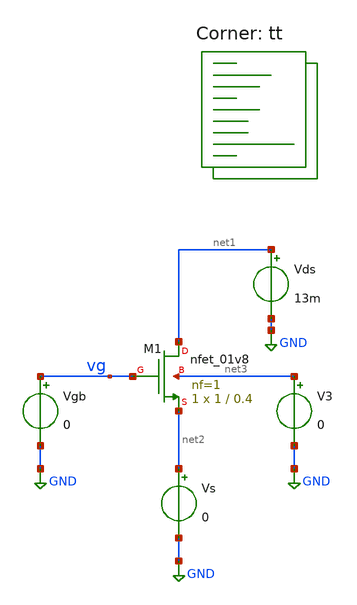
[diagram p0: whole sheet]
** sch_path: legacy/Examples/SkyWater130/xschem/Extraction/nmos_ext.sch
**.subckt nmos_ext
Vgb vg GND 0
Vds net1 GND 13m
V3 net3 GND 0
Vs net2 GND 0
XM1 net1 vg net2 net3 sky130_fd_pr__nfet_01v8 L=0.4 W=1 nf=1 ad='int((nf+1)/2) * W/nf * 0.29' as='int((nf+2)/2) * W/nf * 0.29'
+ pd='2*int((nf+1)/2) * (W/nf + 0.29)' ps='2*int((nf+2)/2) * (W/nf + 0.29)' nrd='0.29 / W' nrs='0.29 / W'
+ sa=0 sb=0 sd=0 mult=1 m=1
**** begin user architecture code
.lib $::SKYWATER_MODELS/sky130.lib.spice tt



.control
  save all
  dc Vgb 0.05 1.8 1m

  let gm_id = deriv(ln(i(Vs)))
  save gm_id

  meas dc gm_id_max MAX gm_id
  let gm_id_vt = 0.531*gm_id_max
  save gm_id_vt

  meas dc vt0 FIND V(vg) WHEN gm_id=gm_id_vt
  meas dc is0_ FIND i(Vs) WHEN V(vg)=vt0

  let is0 = is0_/0.88
  let VT_val=0.026
  let n = 1/(gm_id_max*VT_val)
  save is0 vt0 n
  echo
  echo
  echo

  echo Extracted parameters:
  print is0 vt0 n


  echo
  echo
  echo

  remzerovec
  write nmos_ext.raw
.endc



**** end user architecture code
**.ends
.GLOBAL GND
.end
